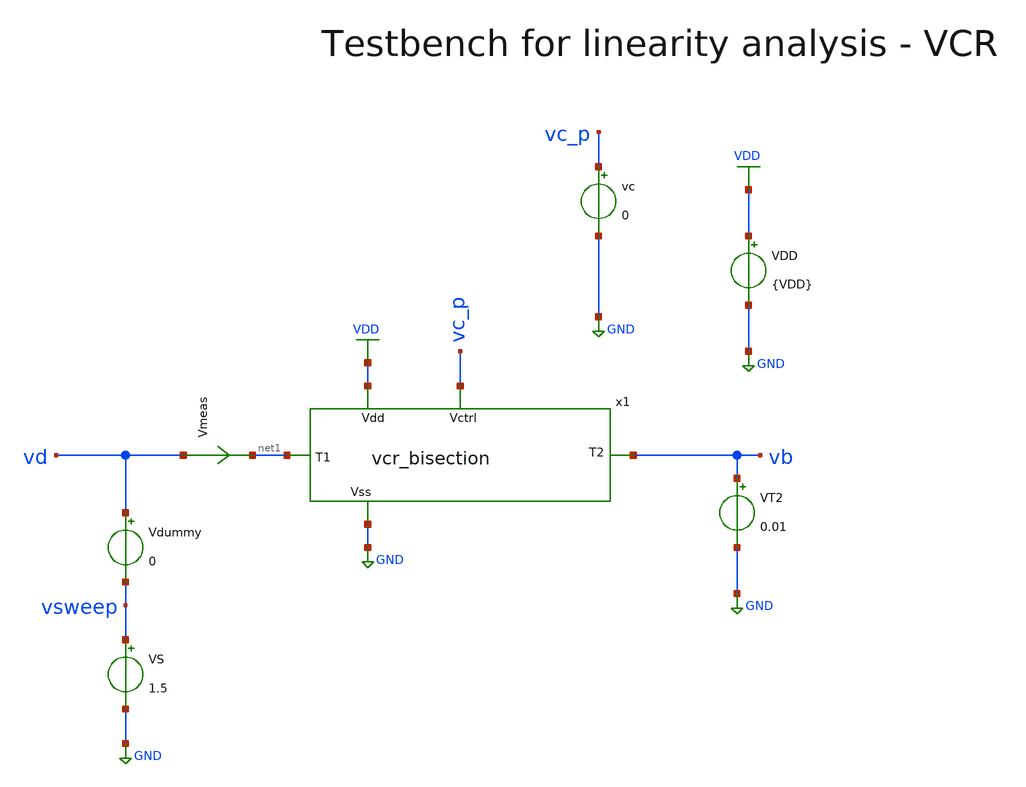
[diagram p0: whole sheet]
** sch_path: macros/voltage_controlled_resistors/macros/vcr_bisection/testbenches/xschem/res_tb_linearity_fix.sch
**.subckt res_tb_linearity_fix
VDD VDD GND {VDD}
VS vsweep GND 1.5
Vmeas vd net1 0
.save i(vmeas)
vc vc_p GND 0
x1 vc_p net1 vb VDD GND vcr_bisection
VT2 vb GND 0.01
Vdummy vd vsweep 0
**** begin user architecture code

.lib cornerMOSlv.lib mos_tt
.lib cornerMOShv.lib mos_tt
.lib cornerRES.lib res_typ
.lib cornerDIO.lib dio_tt
.lib cornerCAP.lib cap_typ



* .include ../../../netlist/pex/inverter_magic_pex_3.spice
.param VDD=3.3
.csparam VDD=VDD
.param Vcm=2.3
.csparam Vcm=Vcm
.param temp=27
.options savecurrents klu method=gear reltol=1e-3 abstol=1e-15 gmin=1e-15 rshunt=1e13
.control
let vcc = 1.5

save all
set appendwrite



repeat 5
  alter vc $&vcc

  * DC Sweep
  dc VS 0.01 3 1m
  remzerovec
  let vcc = vcc + 0.3
end
write @schname\.raw
set appendwrite

* Plotting
plot (dc1.v(vd) - dc1.v(vb))/(dc1.i(vmeas)) (dc2.v(vd) - dc2.v(vb))/(dc2.i(vmeas)) (dc3.v(vd) -
+ dc3.v(vb))/(dc3.i(vmeas)) (dc4.v(vd) - dc4.v(vb))/(dc4.i(vmeas)) (dc5.v(vd) - dc5.v(vb))/(dc5.i(vmeas)) ylimit 0 10k

plot dc1.i(vmeas) dc2.i(vmeas) dc3.i(vmeas) dc4.i(vmeas) dc5.i(vmeas)

* Write Data
unset appendwrite
set wr_vecnames
set wr_singlescale
wrdata ../plot_simulations/data/@schname\.txt v(vc_p) dc1.v(vsweep)/(dc1.i(Vmeas))
+ dc2.v(vsweep)/(dc2.i(Vmeas)) dc3.v(vsweep)/(dc3.i(Vmeas)) dc4.v(vsweep)/(dc4.i(Vmeas)) dc5.v(vsweep)/(dc5.i(Vmeas))

write res_tb_linearity.raw

*quit
.endc


**** end user architecture code
**.ends
.GLOBAL GND
.GLOBAL VDD
.end
